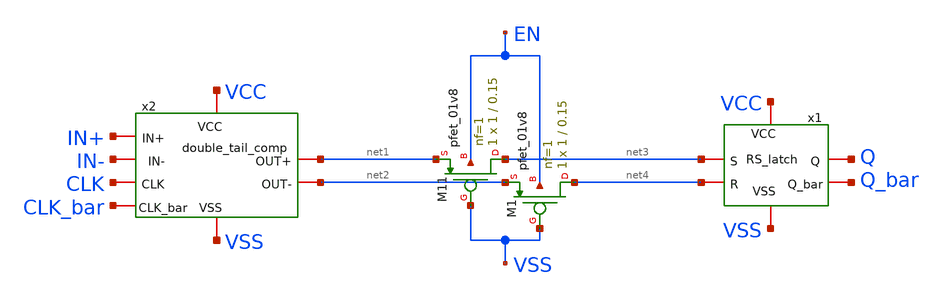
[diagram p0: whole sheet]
** sch_path: temp/comparator_1bit.sch
**.subckt comparator_1bit
x1 VCC net4 net3 Q_bar Q VSS RS_latch
x2 VCC net1 net2 VSS CLK CLK_bar IN+ IN- double_tail_comp
XM11 net3 VSS net1 EN sky130_fd_pr__pfet_01v8 L=0.15 W=1 nf=1 ad='int((nf+1)/2) * W/nf * 0.29' as='int((nf+2)/2) * W/nf * 0.29'
+ pd='2*int((nf+1)/2) * (W/nf + 0.29)' ps='2*int((nf+2)/2) * (W/nf + 0.29)' nrd='0.29 / W' nrs='0.29 / W'
+ sa=0 sb=0 sd=0 mult=1 m=1
XM1 net4 VSS net2 EN sky130_fd_pr__pfet_01v8 L=0.15 W=1 nf=1 ad='int((nf+1)/2) * W/nf * 0.29' as='int((nf+2)/2) * W/nf * 0.29'
+ pd='2*int((nf+1)/2) * (W/nf + 0.29)' ps='2*int((nf+2)/2) * (W/nf + 0.29)' nrd='0.29 / W' nrs='0.29 / W'
+ sa=0 sb=0 sd=0 mult=1 m=1
**.ends

* expanding   symbol:  RS_latch/RS_latch.sym # of pins=6
** sym_path: RS_latch/RS_latch.sym
** sch_path: RS_latch/RS_latch.sch
.subckt RS_latch VCC R S Q_bar Q VSS
*.iopin VCC
*.iopin VSS
*.iopin S
*.iopin R
*.iopin Q
*.iopin Q_bar
XM3 Q Q_bar VCC VCC sky130_fd_pr__pfet_01v8 L=0.15 W=1 nf=1 ad='int((nf+1)/2) * W/nf * 0.29' as='int((nf+2)/2) * W/nf * 0.29'
+ pd='2*int((nf+1)/2) * (W/nf + 0.29)' ps='2*int((nf+2)/2) * (W/nf + 0.29)' nrd='0.29 / W' nrs='0.29 / W'
+ sa=0 sb=0 sd=0 mult=1 m=1
XM1 Q net1 VCC VCC sky130_fd_pr__pfet_01v8 L=0.15 W=1 nf=1 ad='int((nf+1)/2) * W/nf * 0.29' as='int((nf+2)/2) * W/nf * 0.29'
+ pd='2*int((nf+1)/2) * (W/nf + 0.29)' ps='2*int((nf+2)/2) * (W/nf + 0.29)' nrd='0.29 / W' nrs='0.29 / W'
+ sa=0 sb=0 sd=0 mult=1 m=1
XM2 Q_bar net2 VCC VCC sky130_fd_pr__pfet_01v8 L=0.15 W=1 nf=1 ad='int((nf+1)/2) * W/nf * 0.29' as='int((nf+2)/2) * W/nf * 0.29'
+ pd='2*int((nf+1)/2) * (W/nf + 0.29)' ps='2*int((nf+2)/2) * (W/nf + 0.29)' nrd='0.29 / W' nrs='0.29 / W'
+ sa=0 sb=0 sd=0 mult=1 m=1
XM4 Q_bar Q VCC VCC sky130_fd_pr__pfet_01v8 L=0.15 W=1 nf=1 ad='int((nf+1)/2) * W/nf * 0.29' as='int((nf+2)/2) * W/nf * 0.29'
+ pd='2*int((nf+1)/2) * (W/nf + 0.29)' ps='2*int((nf+2)/2) * (W/nf + 0.29)' nrd='0.29 / W' nrs='0.29 / W'
+ sa=0 sb=0 sd=0 mult=1 m=1
XM5 Q net1 D D sky130_fd_pr__nfet_01v8 L=0.15 W=0.5 nf=1 ad='int((1 + 1)/2) * 0.5 / 1 * 0.29' as='int((1 + 2)/2) * 0.5 / 1 * 0.29'
+ pd='2*int((1 + 1)/2) * (0.5 / 1 + 0.29)' ps='2*int((1 + 2)/2) * (0.5 / 1 + 0.29)' nrd='0.29 / 0.5 ' nrs='0.29 / 0.5 '
+ sa=0 sb=0 sd=0 mult=1 m=1
XM6 Q_bar net2 D_bar D_bar sky130_fd_pr__nfet_01v8 L=0.15 W=0.5 nf=1 ad='int((1 + 1)/2) * 0.5 / 1 * 0.29'
+ as='int((1 + 2)/2) * 0.5 / 1 * 0.29' pd='2*int((1 + 1)/2) * (0.5 / 1 + 0.29)' ps='2*int((1 + 2)/2) * (0.5 / 1 + 0.29)'
+ nrd='0.29 / 0.5 ' nrs='0.29 / 0.5 ' sa=0 sb=0 sd=0 mult=1 m=1
XM7 D Q_bar VSS VSS sky130_fd_pr__nfet_01v8 L=0.15 W=0.5 nf=1 ad='int((1 + 1)/2) * 0.5 / 1 * 0.29' as='int((1 + 2)/2) * 0.5 / 1 * 0.29'
+ pd='2*int((1 + 1)/2) * (0.5 / 1 + 0.29)' ps='2*int((1 + 2)/2) * (0.5 / 1 + 0.29)' nrd='0.29 / 0.5 ' nrs='0.29 / 0.5 '
+ sa=0 sb=0 sd=0 mult=1 m=1
XM8 D_bar Q VSS VSS sky130_fd_pr__nfet_01v8 L=0.15 W=0.5 nf=1 ad='int((1 + 1)/2) * 0.5 / 1 * 0.29' as='int((1 + 2)/2) * 0.5 / 1 * 0.29'
+ pd='2*int((1 + 1)/2) * (0.5 / 1 + 0.29)' ps='2*int((1 + 2)/2) * (0.5 / 1 + 0.29)' nrd='0.29 / 0.5 ' nrs='0.29 / 0.5 '
+ sa=0 sb=0 sd=0 mult=1 m=1
XM10 Q_bar S VSS VSS sky130_fd_pr__nfet_01v8 L=0.15 W=1 nf=1 ad='int((1 + 1)/2) * 1 / 1 * 0.29' as='int((1 + 2)/2) * 1 / 1 * 0.29'
+ pd='2*int((1 + 1)/2) * (1 / 1 + 0.29)' ps='2*int((1 + 2)/2) * (1 / 1 + 0.29)' nrd='0.29 / 1 ' nrs='0.29 / 1 '
+ sa=0 sb=0 sd=0 mult=1 m=1
XM9 Q R VSS VSS sky130_fd_pr__nfet_01v8 L=0.15 W=1 nf=1 ad='int((1 + 1)/2) * 1 / 1 * 0.29' as='int((1 + 2)/2) * 1 / 1 * 0.29'
+ pd='2*int((1 + 1)/2) * (1 / 1 + 0.29)' ps='2*int((1 + 2)/2) * (1 / 1 + 0.29)' nrd='0.29 / 1 ' nrs='0.29 / 1 '
+ sa=0 sb=0 sd=0 mult=1 m=1
x1 VCC S net1 VSS inv
x2 VCC R net2 VSS inv
.ends


* expanding   symbol:  voltage_comp/double_tail_comp.sym # of pins=8
** sym_path: voltage_comp/double_tail_comp.sym
** sch_path: voltage_comp/double_tail_comp.sch
.subckt double_tail_comp VCC OUT+ OUT- VSS CLK CLK_bar IN+ IN-
*.iopin OUT-
*.iopin VSS
*.iopin VCC
*.iopin OUT+
*.iopin IN+
*.iopin IN-
*.iopin CLK
*.iopin CLK_bar
XM2 OUT- OUT+ VSS VSS sky130_fd_pr__nfet_01v8 L=0.15 W=0.5 nf=1 ad='int((1 + 1)/2) * 0.5 / 1 * 0.29'
+ as='int((1 + 2)/2) * 0.5 / 1 * 0.29' pd='2*int((1 + 1)/2) * (0.5 / 1 + 0.29)' ps='2*int((1 + 2)/2) * (0.5 / 1 + 0.29)'
+ nrd='0.29 / 0.5 ' nrs='0.29 / 0.5 ' sa=0 sb=0 sd=0 mult=1 m=1
XM11 OUT- OUT+ net2 net2 sky130_fd_pr__pfet_01v8 L=0.15 W=0.5 nf=1 ad='int((nf+1)/2) * W/nf * 0.29' as='int((nf+2)/2) * W/nf * 0.29'
+ pd='2*int((nf+1)/2) * (W/nf + 0.29)' ps='2*int((nf+2)/2) * (W/nf + 0.29)' nrd='0.29 / W' nrs='0.29 / W'
+ sa=0 sb=0 sd=0 mult=1 m=1
XM1 OUT+ OUT- VSS VSS sky130_fd_pr__nfet_01v8 L=0.15 W=0.5 nf=1 ad='int((1 + 1)/2) * 0.5 / 1 * 0.29'
+ as='int((1 + 2)/2) * 0.5 / 1 * 0.29' pd='2*int((1 + 1)/2) * (0.5 / 1 + 0.29)' ps='2*int((1 + 2)/2) * (0.5 / 1 + 0.29)'
+ nrd='0.29 / 0.5 ' nrs='0.29 / 0.5 ' sa=0 sb=0 sd=0 mult=1 m=1
XM3 OUT+ OUT- net2 net2 sky130_fd_pr__pfet_01v8 L=0.15 W=0.5 nf=1 ad='int((nf+1)/2) * W/nf * 0.29' as='int((nf+2)/2) * W/nf * 0.29'
+ pd='2*int((nf+1)/2) * (W/nf + 0.29)' ps='2*int((nf+2)/2) * (W/nf + 0.29)' nrd='0.29 / W' nrs='0.29 / W'
+ sa=0 sb=0 sd=0 mult=1 m=1
XM4 OUT+ Di- VSS VSS sky130_fd_pr__nfet_01v8 L=0.15 W=0.5 nf=1 ad='int((1 + 1)/2) * 0.5 / 1 * 0.29' as='int((1 + 2)/2) * 0.5 / 1 * 0.29'
+ pd='2*int((1 + 1)/2) * (0.5 / 1 + 0.29)' ps='2*int((1 + 2)/2) * (0.5 / 1 + 0.29)' nrd='0.29 / 0.5 ' nrs='0.29 / 0.5 '
+ sa=0 sb=0 sd=0 mult=1 m=1
XM5 OUT- Di+ VSS VSS sky130_fd_pr__nfet_01v8 L=0.15 W=0.5 nf=1 ad='int((1 + 1)/2) * 0.5 / 1 * 0.29' as='int((1 + 2)/2) * 0.5 / 1 * 0.29'
+ pd='2*int((1 + 1)/2) * (0.5 / 1 + 0.29)' ps='2*int((1 + 2)/2) * (0.5 / 1 + 0.29)' nrd='0.29 / 0.5 ' nrs='0.29 / 0.5 '
+ sa=0 sb=0 sd=0 mult=1 m=1
XM6 net2 CLK_bar VCC VCC sky130_fd_pr__pfet_01v8 L=0.15 W=0.5 nf=1 ad='int((nf+1)/2) * W/nf * 0.29' as='int((nf+2)/2) * W/nf * 0.29'
+ pd='2*int((nf+1)/2) * (W/nf + 0.29)' ps='2*int((nf+2)/2) * (W/nf + 0.29)' nrd='0.29 / W' nrs='0.29 / W'
+ sa=0 sb=0 sd=0 mult=1 m=1
XM8 Di- CLK VCC VCC sky130_fd_pr__pfet_01v8 L=0.15 W=1 nf=1 ad='int((nf+1)/2) * W/nf * 0.29' as='int((nf+2)/2) * W/nf * 0.29'
+ pd='2*int((nf+1)/2) * (W/nf + 0.29)' ps='2*int((nf+2)/2) * (W/nf + 0.29)' nrd='0.29 / W' nrs='0.29 / W'
+ sa=0 sb=0 sd=0 mult=1 m=1
XM9 Di- IN+ net1 net1 sky130_fd_pr__nfet_01v8 L=0.15 W=1 nf=1 ad='int((1 + 1)/2) * 1 / 1 * 0.29' as='int((1 + 2)/2) * 1 / 1 * 0.29'
+ pd='2*int((1 + 1)/2) * (1 / 1 + 0.29)' ps='2*int((1 + 2)/2) * (1 / 1 + 0.29)' nrd='0.29 / 1 ' nrs='0.29 / 1 '
+ sa=0 sb=0 sd=0 mult=1 m=1
XM7 Di+ CLK VCC VCC sky130_fd_pr__pfet_01v8 L=0.15 W=1 nf=1 ad='int((nf+1)/2) * W/nf * 0.29' as='int((nf+2)/2) * W/nf * 0.29'
+ pd='2*int((nf+1)/2) * (W/nf + 0.29)' ps='2*int((nf+2)/2) * (W/nf + 0.29)' nrd='0.29 / W' nrs='0.29 / W'
+ sa=0 sb=0 sd=0 mult=1 m=1
XM10 Di+ IN- net1 net1 sky130_fd_pr__nfet_01v8 L=0.15 W=1 nf=1 ad='int((1 + 1)/2) * 1 / 1 * 0.29' as='int((1 + 2)/2) * 1 / 1 * 0.29'
+ pd='2*int((1 + 1)/2) * (1 / 1 + 0.29)' ps='2*int((1 + 2)/2) * (1 / 1 + 0.29)' nrd='0.29 / 1 ' nrs='0.29 / 1 '
+ sa=0 sb=0 sd=0 mult=1 m=1
XM12 net1 CLK VSS VSS sky130_fd_pr__nfet_01v8 L=0.15 W=1 nf=1 ad='int((1 + 1)/2) * 1 / 1 * 0.29' as='int((1 + 2)/2) * 1 / 1 * 0.29'
+ pd='2*int((1 + 1)/2) * (1 / 1 + 0.29)' ps='2*int((1 + 2)/2) * (1 / 1 + 0.29)' nrd='0.29 / 1 ' nrs='0.29 / 1 '
+ sa=0 sb=0 sd=0 mult=1 m=1
.ends


* expanding   symbol:  inv.sym # of pins=4
** sym_path: temp/inv.sym
** sch_path: temp/inv.sch
.subckt inv VCC IN OUT VSS
*.iopin VCC
*.iopin IN
*.iopin OUT
*.iopin VSS
XM1 OUT IN VSS VSS sky130_fd_pr__nfet_01v8 L=0.15 W=0.5 nf=1 ad='int((nf+1)/2) * W/nf * 0.29' as='int((nf+2)/2) * W/nf * 0.29'
+ pd='2*int((nf+1)/2) * (W/nf + 0.29)' ps='2*int((nf+2)/2) * (W/nf + 0.29)' nrd='0.29 / W' nrs='0.29 / W'
+ sa=0 sb=0 sd=0 mult=1 m=1
XM2 OUT IN VCC VCC sky130_fd_pr__pfet_01v8 L=0.15 W=1.05 nf=1 ad='int((nf+1)/2) * W/nf * 0.29' as='int((nf+2)/2) * W/nf * 0.29'
+ pd='2*int((nf+1)/2) * (W/nf + 0.29)' ps='2*int((nf+2)/2) * (W/nf + 0.29)' nrd='0.29 / W' nrs='0.29 / W'
+ sa=0 sb=0 sd=0 mult=1 m=1
.ends

.end
